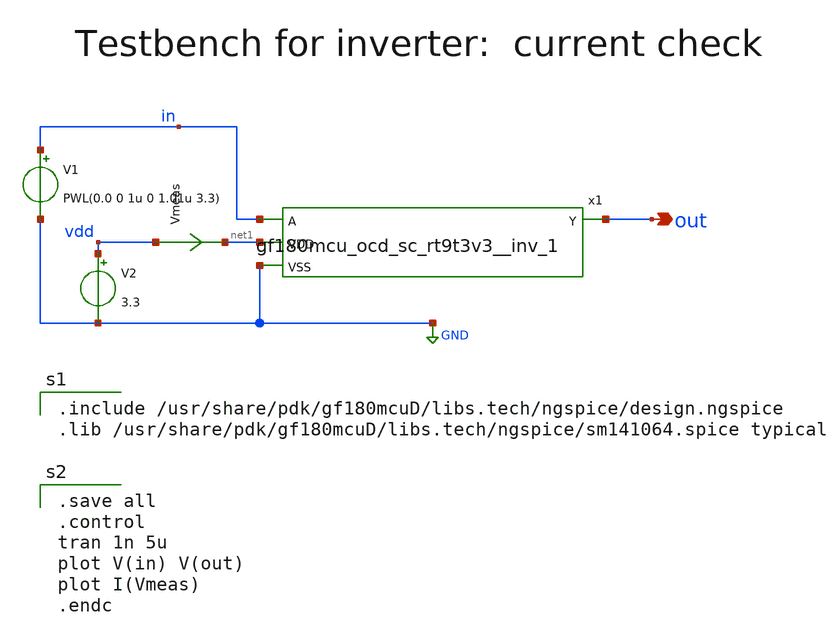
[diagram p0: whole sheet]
** sch_path: xschem/test_tb.sch
**.subckt test_tb out
*.opin out
V1 in GND PWL(0.0 0 1u 0 1.01u 3.3)
V2 vdd GND 3.3
x1 in out net1 GND gf180mcu_ocd_sc_rt9t3v3__inv_1
Vmeas vdd net1 0
.save i(vmeas)
**** begin user architecture code

.save all
.control
tran 1n 5u
plot V(in) V(out)
plot I(Vmeas)
.endc


.include /usr/share/pdk/gf180mcuD/libs.tech/ngspice/design.ngspice
.lib /usr/share/pdk/gf180mcuD/libs.tech/ngspice/sm141064.spice typical

**** end user architecture code
**.ends
.GLOBAL GND
.end
